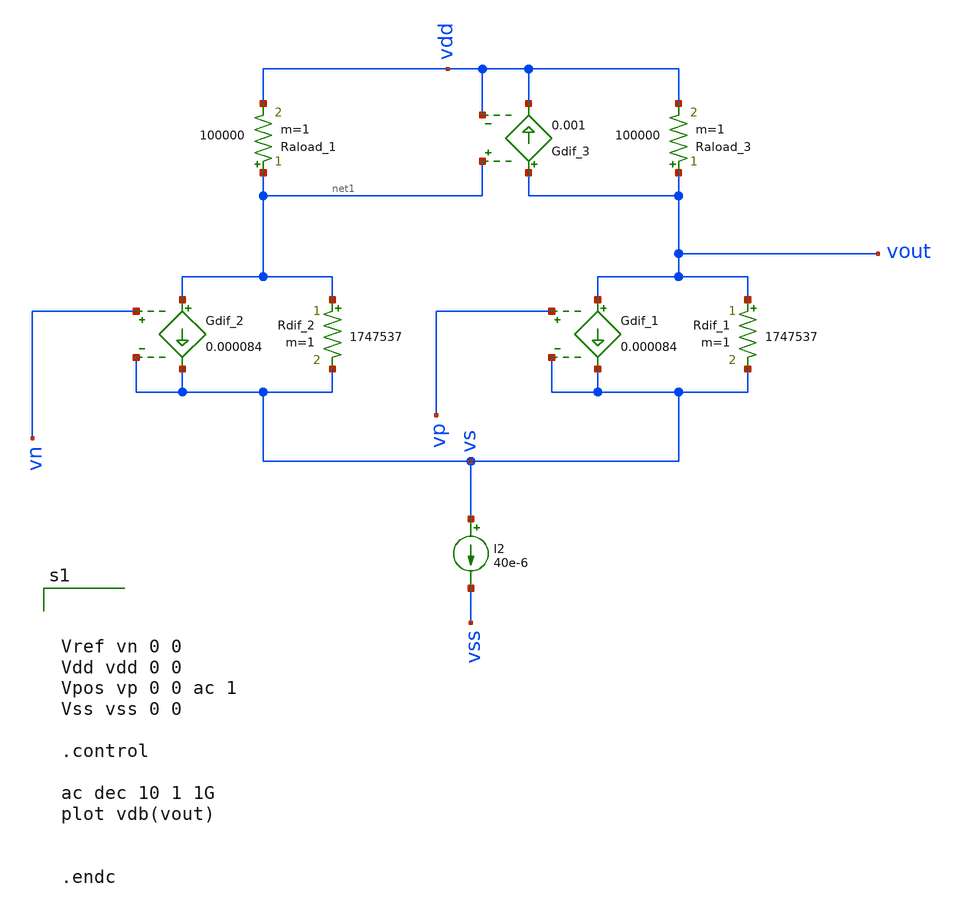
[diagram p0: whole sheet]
** sch_path: test-python/result_comp/xschem/ota_tb.sch
**.subckt ota_tb
Rdif_2 net1 vs 1747537 m=1
Gdif_2 net1 vs vn vs 0.000084
Rdif_1 vout vs 1747537 m=1
Gdif_1 vout vs vp vs 0.000084
I2 vs vss 40e-6
Raload_3 vout vdd 100000 m=1
Raload_1 net1 vdd 100000 m=1
Gdif_3 vout vdd net1 vdd 0.001
**** begin user architecture code



Vref vn 0 0
Vdd vdd 0 0
Vpos vp 0 0 ac 1
Vss vss 0 0

.control

ac dec 10 1 1G
plot vdb(vout)


.endc



**** end user architecture code
**.ends
.end
